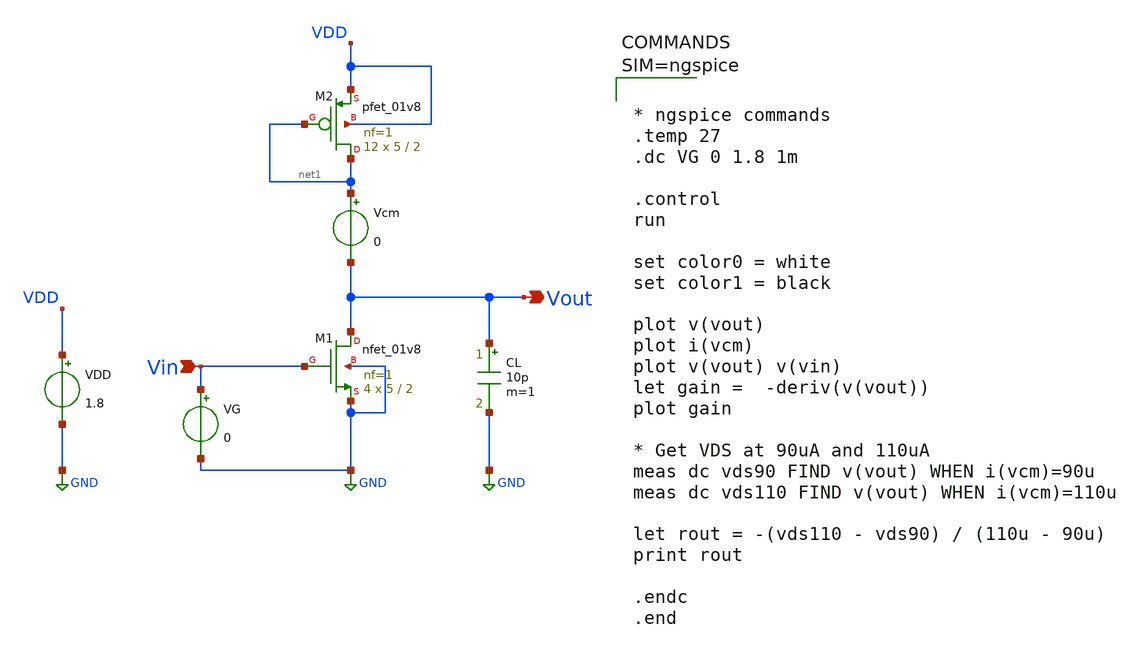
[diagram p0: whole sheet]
** sch_path: Common_Source_PMOS_Load_ckts/CS_Amp_PMOS_Diode_Load_Ckts/NMOS_PMOS_Diode_Load_DC_Sweep.sch
**.subckt NMOS_PMOS_Diode_Load_DC_Sweep Vout Vin
*.opin Vout
*.ipin Vin
XM1 Vout Vin GND GND sky130_fd_pr__nfet_01v8 L=2 W=5 nf=1 ad='int((1 + 1)/2) * 5 / 1 * 0.29' as='int((1 + 2)/2) * 5 / 1 * 0.29'
+ pd='2*int((1 + 1)/2) * (5 / 1 + 0.29)' ps='2*int((1 + 2)/2) * (5 / 1 + 0.29)' nrd='0.29 / 5 ' nrs='0.29 / 5 '
+ sa=0 sb=0 sd=0 mult=4 m=4
XM2 net1 net1 VDD VDD sky130_fd_pr__pfet_01v8 L=2 W=5 nf=1 ad='int((1 + 1)/2) * 5 / 1 * 0.29' as='int((1 + 2)/2) * 5 / 1 * 0.29'
+ pd='2*int((1 + 1)/2) * (5 / 1 + 0.29)' ps='2*int((1 + 2)/2) * (5 / 1 + 0.29)' nrd='0.29 / 5 ' nrs='0.29 / 5 '
+ sa=0 sb=0 sd=0 mult=12 m=12
Vcm net1 Vout 0
CL Vout GND 10p m=1
VG Vin GND 0
VDD VDD GND 1.8
**** begin user architecture code

** opencircuitdesign pdks install
.lib $::SKYWATER_MODELS/sky130.lib.spice tt




* ngspice commands
.temp 27
.dc VG 0 1.8 1m

.control
run

set color0 = white
set color1 = black

plot v(vout)
plot i(vcm)
plot v(vout) v(vin)
let gain =  -deriv(v(vout))
plot gain

* Get VDS at 90uA and 110uA
meas dc vds90 FIND v(vout) WHEN i(vcm)=90u
meas dc vds110 FIND v(vout) WHEN i(vcm)=110u

let rout = -(vds110 - vds90) / (110u - 90u)
print rout

.endc
.end



**** end user architecture code
**.ends
.GLOBAL GND
.end
